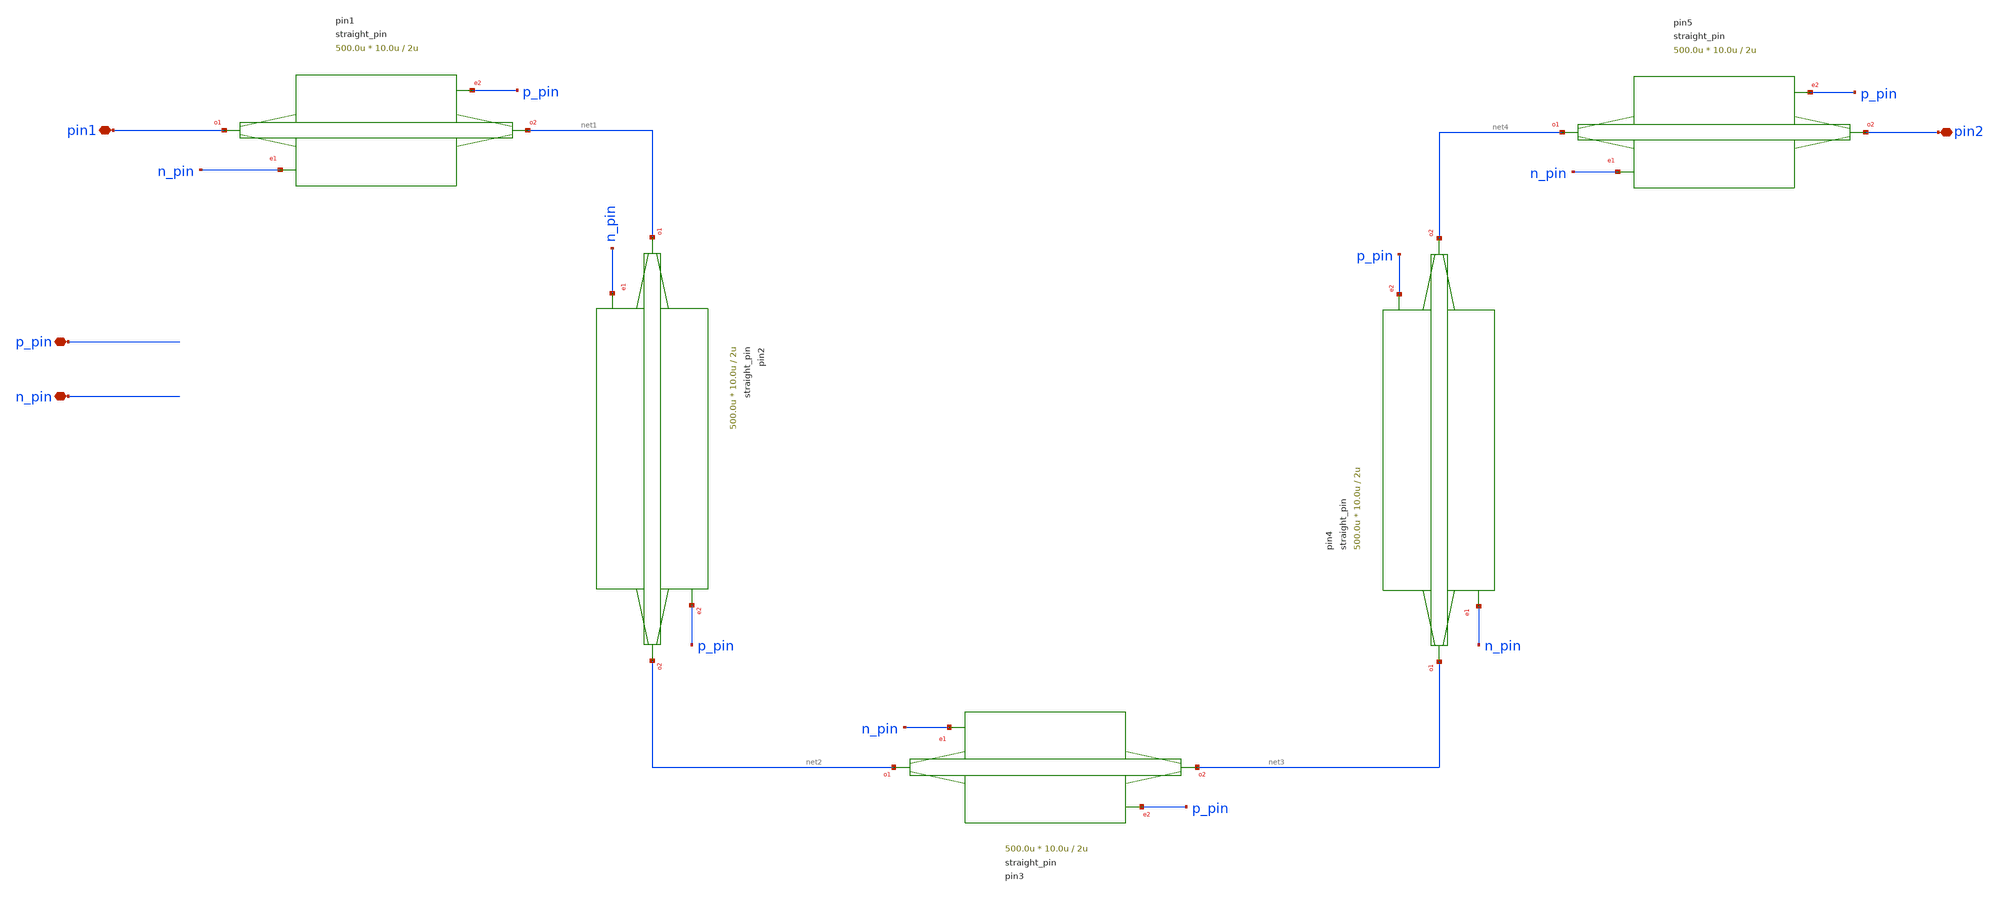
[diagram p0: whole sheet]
** sch_path: xschem/tests/test_sch/test_straight_pin.sch
* Copyright (c) 2024, Mabrains LLC
* Licensed under the GNU Lesser General Public License, Version 3.0 (the "License");
* you may not use this file except in compliance with the License.
* GNU Lesser General Public License
* Version 3, 29 June 2007
* This program is free software: you can redistribute it and/or modify
* it under the terms of the GNU Lesser General Public License as published
* by the Free Software Foundation, either version 3 of the License, or
* (at your option) any later version.
* This program is distributed in the hope that it will be useful,
* but WITHOUT ANY WARRANTY; without even the implied warranty of
* MERCHANTABILITY or FITNESS FOR A PARTICULAR PURPOSE.  See the
* GNU Lesser General Public License for more details.
* You should have received a copy of the GNU Lesser General Public License
* along with this program.  If not, see <https://www.gnu.org/licenses/>.
* SPDX-License-Identifier: LGPL-3.0
**.subckt test_straight_pin pin1 pin2 p_pin n_pin
*.iopin pin1
*.iopin pin2
*.iopin p_pin
*.iopin n_pin
Ppin1 pin1 net1 n_pin p_pin straight_pin length=500.0u via_stack_width=10.0u via_stack_spacing=2u
Ppin2 net1 net2 n_pin p_pin straight_pin length=500.0u via_stack_width=10.0u via_stack_spacing=2u
Ppin3 net2 net3 n_pin p_pin straight_pin length=500.0u via_stack_width=10.0u via_stack_spacing=2u
Ppin4 net3 net4 n_pin p_pin straight_pin length=500.0u via_stack_width=10.0u via_stack_spacing=2u
Ppin5 net4 pin2 n_pin p_pin straight_pin length=500.0u via_stack_width=10.0u via_stack_spacing=2u
**.ends
.end
